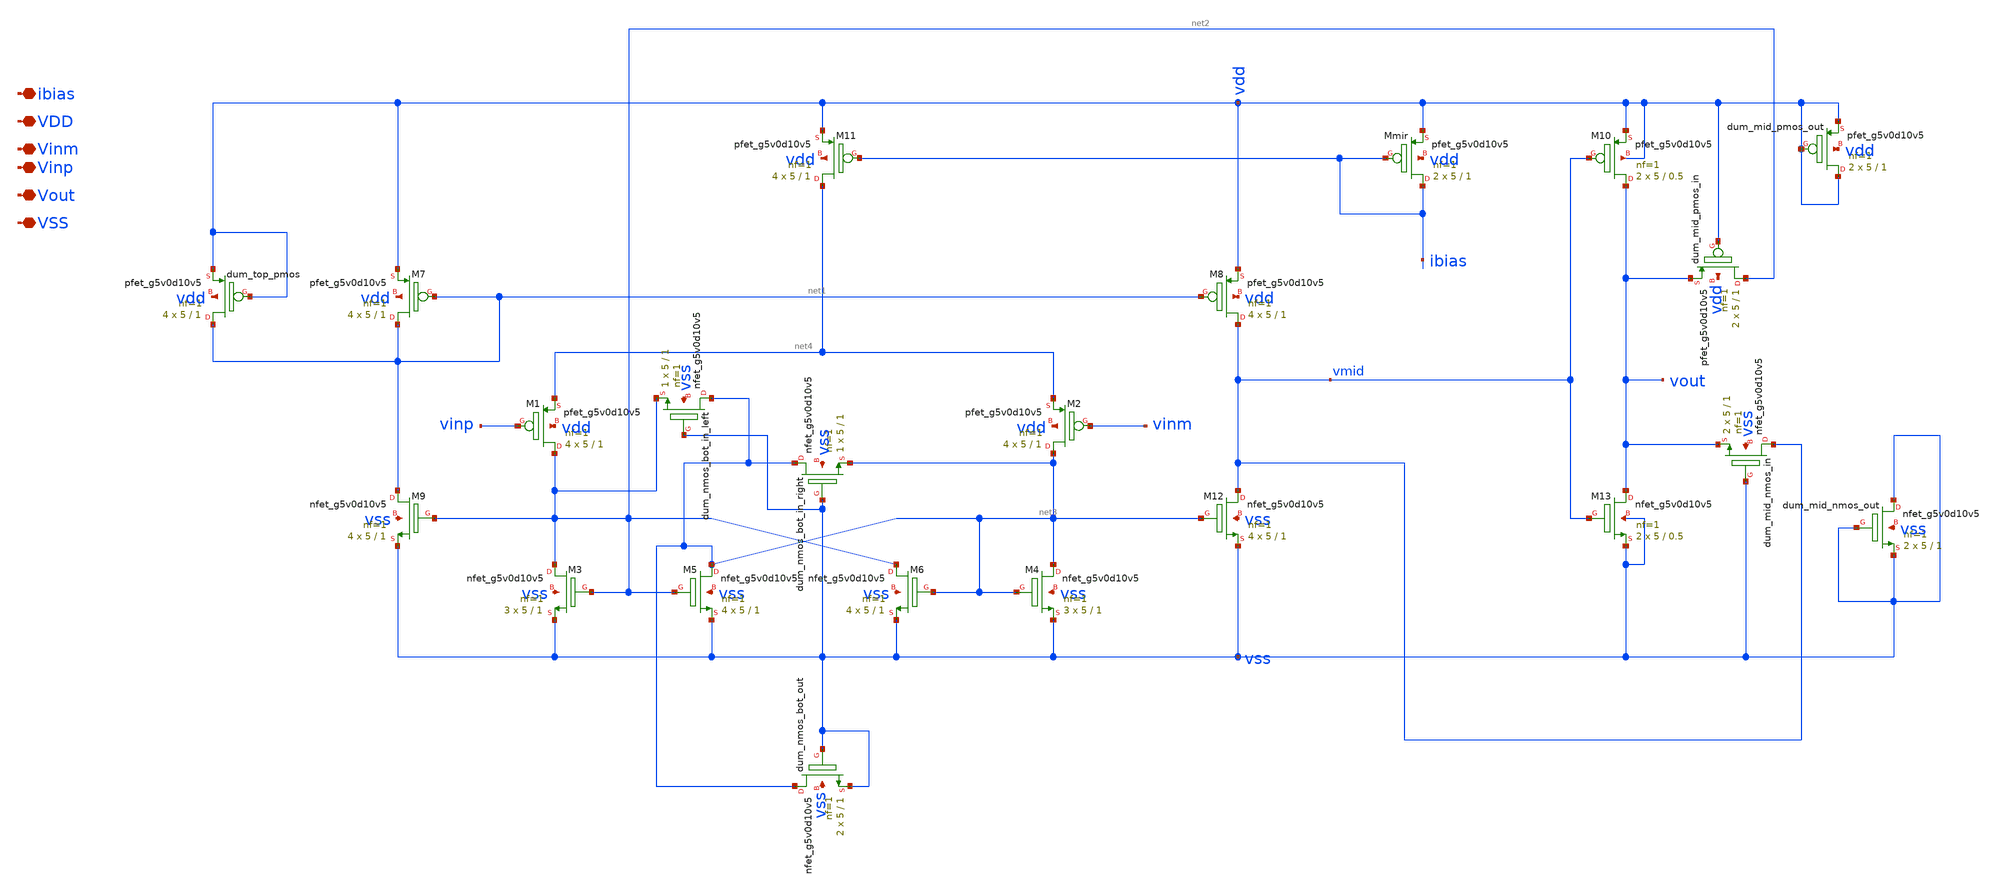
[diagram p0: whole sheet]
** sch_path: images/foss-asic-tools/addons/examples/Open-PMIC-tapeout/xschem/comparator_w_obuff.sch
**.subckt comparator_w_obuff ibias VDD Vinm Vinp Vout VSS
*.iopin ibias
*.iopin VDD
*.iopin Vinm
*.iopin Vinp
*.iopin Vout
*.iopin VSS
XM1 net2 vinp net4 vdd sky130_fd_pr__pfet_g5v0d10v5 L=1 W=5 nf=1 ad='int((nf+1)/2) * W/nf * 0.29' as='int((nf+2)/2) * W/nf * 0.29'
+ pd='2*int((nf+1)/2) * (W/nf + 0.29)' ps='2*int((nf+2)/2) * (W/nf + 0.29)' nrd='0.29 / W' nrs='0.29 / W'
+ sa=0 sb=0 sd=0 mult=4 m=4
XM2 net3 vinm net4 vdd sky130_fd_pr__pfet_g5v0d10v5 L=1 W=5 nf=1 ad='int((nf+1)/2) * W/nf * 0.29' as='int((nf+2)/2) * W/nf * 0.29'
+ pd='2*int((nf+1)/2) * (W/nf + 0.29)' ps='2*int((nf+2)/2) * (W/nf + 0.29)' nrd='0.29 / W' nrs='0.29 / W'
+ sa=0 sb=0 sd=0 mult=4 m=4
XM7 net1 net1 vdd vdd sky130_fd_pr__pfet_g5v0d10v5 L=1 W=5 nf=1 ad='int((nf+1)/2) * W/nf * 0.29' as='int((nf+2)/2) * W/nf * 0.29'
+ pd='2*int((nf+1)/2) * (W/nf + 0.29)' ps='2*int((nf+2)/2) * (W/nf + 0.29)' nrd='0.29 / W' nrs='0.29 / W'
+ sa=0 sb=0 sd=0 mult=4 m=4
XM8 vmid net1 vdd vdd sky130_fd_pr__pfet_g5v0d10v5 L=1 W=5 nf=1 ad='int((nf+1)/2) * W/nf * 0.29' as='int((nf+2)/2) * W/nf * 0.29'
+ pd='2*int((nf+1)/2) * (W/nf + 0.29)' ps='2*int((nf+2)/2) * (W/nf + 0.29)' nrd='0.29 / W' nrs='0.29 / W'
+ sa=0 sb=0 sd=0 mult=4 m=4
XM11 net4 ibias vdd vdd sky130_fd_pr__pfet_g5v0d10v5 L=1 W=5 nf=1 ad='int((nf+1)/2) * W/nf * 0.29' as='int((nf+2)/2) * W/nf * 0.29'
+ pd='2*int((nf+1)/2) * (W/nf + 0.29)' ps='2*int((nf+2)/2) * (W/nf + 0.29)' nrd='0.29 / W' nrs='0.29 / W'
+ sa=0 sb=0 sd=0 mult=4 m=4
XMmir ibias ibias vdd vdd sky130_fd_pr__pfet_g5v0d10v5 L=1 W=5 nf=1 ad='int((nf+1)/2) * W/nf * 0.29'
+ as='int((nf+2)/2) * W/nf * 0.29' pd='2*int((nf+1)/2) * (W/nf + 0.29)' ps='2*int((nf+2)/2) * (W/nf + 0.29)'
+ nrd='0.29 / W' nrs='0.29 / W' sa=0 sb=0 sd=0 mult=2 m=2
XM12 vmid net3 vss vss sky130_fd_pr__nfet_g5v0d10v5 L=1 W=5 nf=1 ad='int((nf+1)/2) * W/nf * 0.29' as='int((nf+2)/2) * W/nf * 0.29'
+ pd='2*int((nf+1)/2) * (W/nf + 0.29)' ps='2*int((nf+2)/2) * (W/nf + 0.29)' nrd='0.29 / W' nrs='0.29 / W'
+ sa=0 sb=0 sd=0 mult=4 m=4
XM4 net3 net3 vss vss sky130_fd_pr__nfet_g5v0d10v5 L=1 W=5 nf=1 ad='int((nf+1)/2) * W/nf * 0.29' as='int((nf+2)/2) * W/nf * 0.29'
+ pd='2*int((nf+1)/2) * (W/nf + 0.29)' ps='2*int((nf+2)/2) * (W/nf + 0.29)' nrd='0.29 / W' nrs='0.29 / W'
+ sa=0 sb=0 sd=0 mult=3 m=3
XM6 net2 net3 vss vss sky130_fd_pr__nfet_g5v0d10v5 L=1 W=5 nf=1 ad='int((nf+1)/2) * W/nf * 0.29' as='int((nf+2)/2) * W/nf * 0.29'
+ pd='2*int((nf+1)/2) * (W/nf + 0.29)' ps='2*int((nf+2)/2) * (W/nf + 0.29)' nrd='0.29 / W' nrs='0.29 / W'
+ sa=0 sb=0 sd=0 mult=4 m=4
XM5 net3 net2 vss vss sky130_fd_pr__nfet_g5v0d10v5 L=1 W=5 nf=1 ad='int((nf+1)/2) * W/nf * 0.29' as='int((nf+2)/2) * W/nf * 0.29'
+ pd='2*int((nf+1)/2) * (W/nf + 0.29)' ps='2*int((nf+2)/2) * (W/nf + 0.29)' nrd='0.29 / W' nrs='0.29 / W'
+ sa=0 sb=0 sd=0 mult=4 m=4
XM3 net2 net2 vss vss sky130_fd_pr__nfet_g5v0d10v5 L=1 W=5 nf=1 ad='int((nf+1)/2) * W/nf * 0.29' as='int((nf+2)/2) * W/nf * 0.29'
+ pd='2*int((nf+1)/2) * (W/nf + 0.29)' ps='2*int((nf+2)/2) * (W/nf + 0.29)' nrd='0.29 / W' nrs='0.29 / W'
+ sa=0 sb=0 sd=0 mult=3 m=3
XM9 net1 net2 vss vss sky130_fd_pr__nfet_g5v0d10v5 L=1 W=5 nf=1 ad='int((nf+1)/2) * W/nf * 0.29' as='int((nf+2)/2) * W/nf * 0.29'
+ pd='2*int((nf+1)/2) * (W/nf + 0.29)' ps='2*int((nf+2)/2) * (W/nf + 0.29)' nrd='0.29 / W' nrs='0.29 / W'
+ sa=0 sb=0 sd=0 mult=4 m=4
XM10 vout vmid vdd vdd sky130_fd_pr__pfet_g5v0d10v5 L=0.5 W=5 nf=1 ad='int((nf+1)/2) * W/nf * 0.29' as='int((nf+2)/2) * W/nf * 0.29'
+ pd='2*int((nf+1)/2) * (W/nf + 0.29)' ps='2*int((nf+2)/2) * (W/nf + 0.29)' nrd='0.29 / W' nrs='0.29 / W'
+ sa=0 sb=0 sd=0 mult=2 m=2
XM13 vout vmid vss vss sky130_fd_pr__nfet_g5v0d10v5 L=0.5 W=5 nf=1 ad='int((nf+1)/2) * W/nf * 0.29' as='int((nf+2)/2) * W/nf * 0.29'
+ pd='2*int((nf+1)/2) * (W/nf + 0.29)' ps='2*int((nf+2)/2) * (W/nf + 0.29)' nrd='0.29 / W' nrs='0.29 / W'
+ sa=0 sb=0 sd=0 mult=2 m=2
Xdum_top_pmos net1 vdd vdd vdd sky130_fd_pr__pfet_g5v0d10v5 L=1 W=5 nf=1 ad='int((nf+1)/2) * W/nf * 0.29'
+ as='int((nf+2)/2) * W/nf * 0.29' pd='2*int((nf+1)/2) * (W/nf + 0.29)' ps='2*int((nf+2)/2) * (W/nf + 0.29)'
+ nrd='0.29 / W' nrs='0.29 / W' sa=0 sb=0 sd=0 mult=4 m=4
Xdum_mid_pmos_out vdd vdd vdd vdd sky130_fd_pr__pfet_g5v0d10v5 L=1 W=5 nf=1 ad='int((nf+1)/2) * W/nf * 0.29'
+ as='int((nf+2)/2) * W/nf * 0.29' pd='2*int((nf+1)/2) * (W/nf + 0.29)' ps='2*int((nf+2)/2) * (W/nf + 0.29)'
+ nrd='0.29 / W' nrs='0.29 / W' sa=0 sb=0 sd=0 mult=2 m=2
Xdum_mid_pmos_in net2 vdd vout vdd sky130_fd_pr__pfet_g5v0d10v5 L=1 W=5 nf=1 ad='int((nf+1)/2) * W/nf * 0.29'
+ as='int((nf+2)/2) * W/nf * 0.29' pd='2*int((nf+1)/2) * (W/nf + 0.29)' ps='2*int((nf+2)/2) * (W/nf + 0.29)'
+ nrd='0.29 / W' nrs='0.29 / W' sa=0 sb=0 sd=0 mult=2 m=2
Xdum_mid_nmos_out vss vss vss vss sky130_fd_pr__nfet_g5v0d10v5 L=1 W=5 nf=1 ad='int((nf+1)/2) * W/nf * 0.29'
+ as='int((nf+2)/2) * W/nf * 0.29' pd='2*int((nf+1)/2) * (W/nf + 0.29)' ps='2*int((nf+2)/2) * (W/nf + 0.29)'
+ nrd='0.29 / W' nrs='0.29 / W' sa=0 sb=0 sd=0 mult=2 m=2
Xdum_mid_nmos_in vmid vss vout vss sky130_fd_pr__nfet_g5v0d10v5 L=1 W=5 nf=1 ad='int((nf+1)/2) * W/nf * 0.29'
+ as='int((nf+2)/2) * W/nf * 0.29' pd='2*int((nf+1)/2) * (W/nf + 0.29)' ps='2*int((nf+2)/2) * (W/nf + 0.29)'
+ nrd='0.29 / W' nrs='0.29 / W' sa=0 sb=0 sd=0 mult=2 m=2
Xdum_nmos_bot_in_right net3 vss net3 vss sky130_fd_pr__nfet_g5v0d10v5 L=1 W=5 nf=1 ad='int((nf+1)/2) * W/nf * 0.29'
+ as='int((nf+2)/2) * W/nf * 0.29' pd='2*int((nf+1)/2) * (W/nf + 0.29)' ps='2*int((nf+2)/2) * (W/nf + 0.29)'
+ nrd='0.29 / W' nrs='0.29 / W' sa=0 sb=0 sd=0 mult=1 m=1
Xdum_nmos_bot_out net3 vss vss vss sky130_fd_pr__nfet_g5v0d10v5 L=1 W=5 nf=1 ad='int((nf+1)/2) * W/nf * 0.29'
+ as='int((nf+2)/2) * W/nf * 0.29' pd='2*int((nf+1)/2) * (W/nf + 0.29)' ps='2*int((nf+2)/2) * (W/nf + 0.29)'
+ nrd='0.29 / W' nrs='0.29 / W' sa=0 sb=0 sd=0 mult=2 m=2
Xdum_nmos_bot_in_left net3 vss net2 vss sky130_fd_pr__nfet_g5v0d10v5 L=1 W=5 nf=1 ad='int((nf+1)/2) * W/nf * 0.29'
+ as='int((nf+2)/2) * W/nf * 0.29' pd='2*int((nf+1)/2) * (W/nf + 0.29)' ps='2*int((nf+2)/2) * (W/nf + 0.29)'
+ nrd='0.29 / W' nrs='0.29 / W' sa=0 sb=0 sd=0 mult=1 m=1
**.ends
.end
